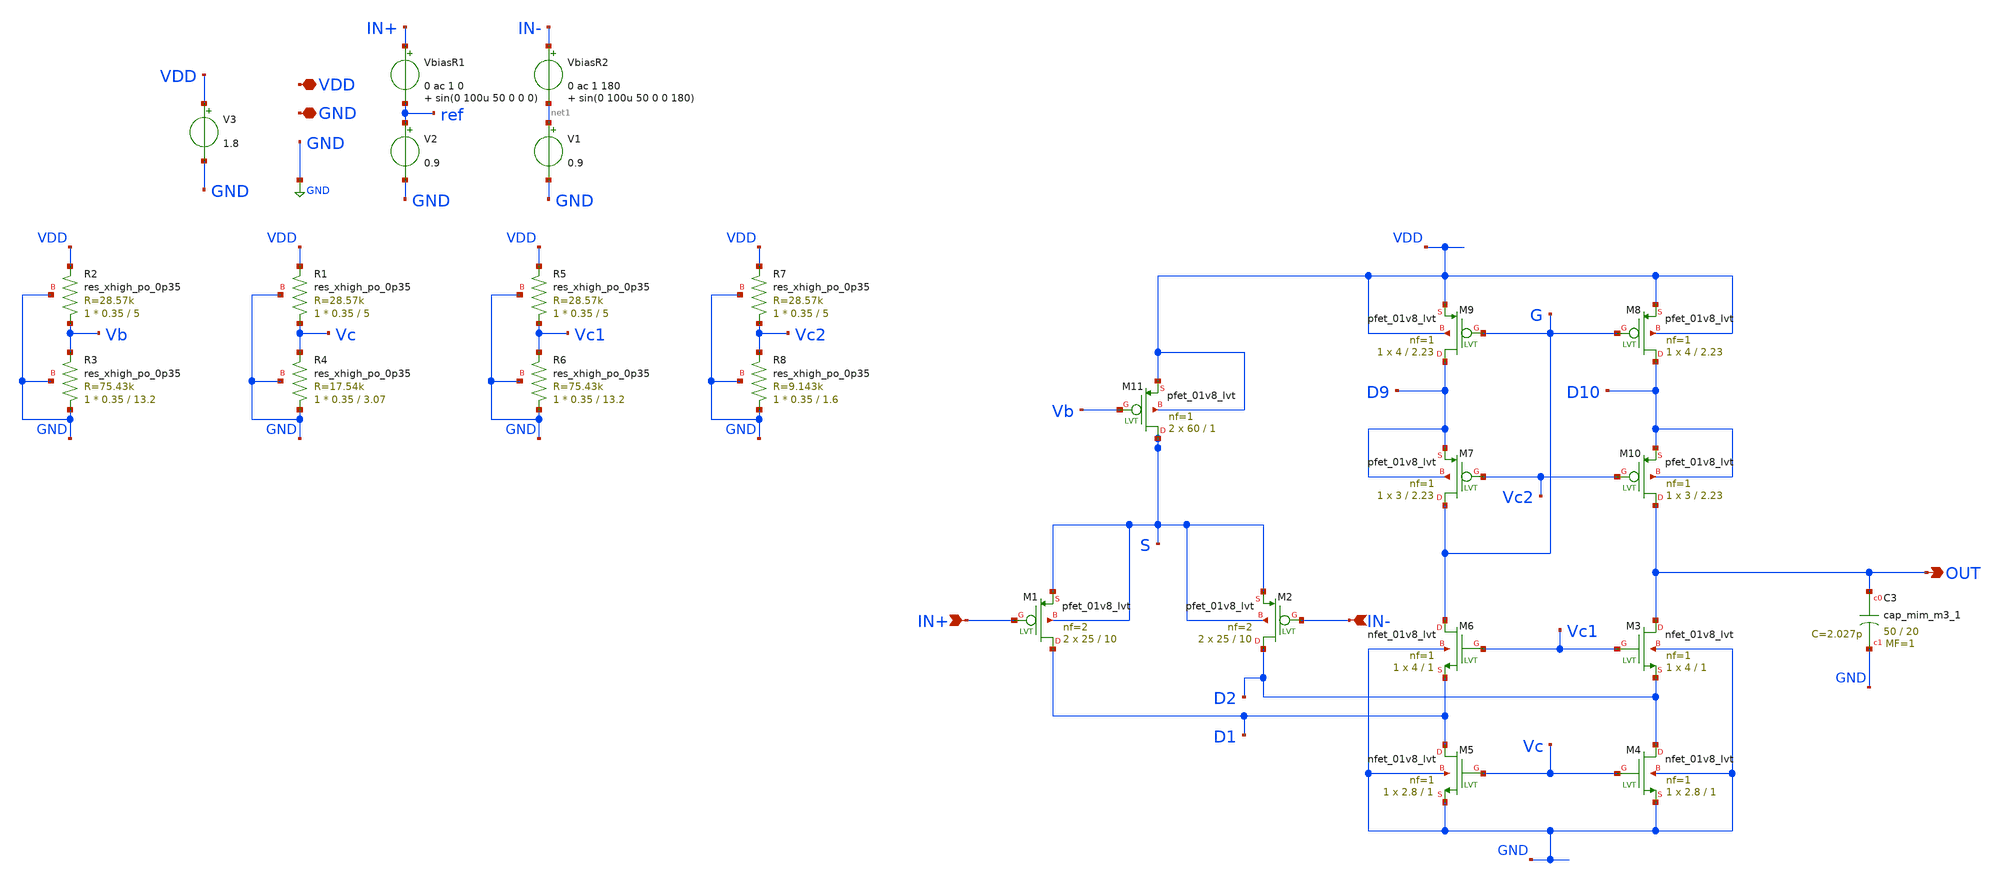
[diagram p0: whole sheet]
** sch_path: xschem/OTA_FoldedCascode_AC1_PVT.sch
**.subckt OTA_FoldedCascode_AC1_PVT VDD GND OUT IN+ IN-
*.iopin VDD
*.iopin GND
*.opin OUT
*.ipin IN+
*.ipin IN-
VbiasR1 IN+ ref 0 ac 1 0 sin(0 100u 50 0 0 0)
V2 ref GND 0.9
V3 VDD GND 1.8
XC3 OUT GND sky130_fd_pr__cap_mim_m3_1 W=50 L=20 MF=1 m=1
XM11 S Vb VDD VDD sky130_fd_pr__pfet_01v8_lvt L=1 W=60 nf=1 ad='int((nf+1)/2) * W/nf * 0.29' as='int((nf+2)/2) * W/nf * 0.29'
+ pd='2*int((nf+1)/2) * (W/nf + 0.29)' ps='2*int((nf+2)/2) * (W/nf + 0.29)' nrd='0.29 / W' nrs='0.29 / W'
+ sa=0 sb=0 sd=0 mult=2 m=2
XM1 D1 IN+ S S sky130_fd_pr__pfet_01v8_lvt L=10 W=25 nf=2 ad='int((nf+1)/2) * W/nf * 0.29' as='int((nf+2)/2) * W/nf * 0.29'
+ pd='2*int((nf+1)/2) * (W/nf + 0.29)' ps='2*int((nf+2)/2) * (W/nf + 0.29)' nrd='0.29 / W' nrs='0.29 / W'
+ sa=0 sb=0 sd=0 mult=2 m=2
XM2 D2 IN- S S sky130_fd_pr__pfet_01v8_lvt L=10 W=25 nf=2 ad='int((nf+1)/2) * W/nf * 0.29' as='int((nf+2)/2) * W/nf * 0.29'
+ pd='2*int((nf+1)/2) * (W/nf + 0.29)' ps='2*int((nf+2)/2) * (W/nf + 0.29)' nrd='0.29 / W' nrs='0.29 / W'
+ sa=0 sb=0 sd=0 mult=2 m=2
XM3 OUT Vc1 D2 GND sky130_fd_pr__nfet_01v8_lvt L=1 W=4 nf=1 ad='int((nf+1)/2) * W/nf * 0.29' as='int((nf+2)/2) * W/nf * 0.29'
+ pd='2*int((nf+1)/2) * (W/nf + 0.29)' ps='2*int((nf+2)/2) * (W/nf + 0.29)' nrd='0.29 / W' nrs='0.29 / W'
+ sa=0 sb=0 sd=0 mult=1 m=1
XM4 D2 Vc GND GND sky130_fd_pr__nfet_01v8_lvt L=1 W=2.8 nf=1 ad='int((nf+1)/2) * W/nf * 0.29' as='int((nf+2)/2) * W/nf * 0.29'
+ pd='2*int((nf+1)/2) * (W/nf + 0.29)' ps='2*int((nf+2)/2) * (W/nf + 0.29)' nrd='0.29 / W' nrs='0.29 / W'
+ sa=0 sb=0 sd=0 mult=1 m=1
XM5 D1 Vc GND GND sky130_fd_pr__nfet_01v8_lvt L=1 W=2.8 nf=1 ad='int((nf+1)/2) * W/nf * 0.29' as='int((nf+2)/2) * W/nf * 0.29'
+ pd='2*int((nf+1)/2) * (W/nf + 0.29)' ps='2*int((nf+2)/2) * (W/nf + 0.29)' nrd='0.29 / W' nrs='0.29 / W'
+ sa=0 sb=0 sd=0 mult=1 m=1
XM6 G Vc1 D1 GND sky130_fd_pr__nfet_01v8_lvt L=1 W=4 nf=1 ad='int((nf+1)/2) * W/nf * 0.29' as='int((nf+2)/2) * W/nf * 0.29'
+ pd='2*int((nf+1)/2) * (W/nf + 0.29)' ps='2*int((nf+2)/2) * (W/nf + 0.29)' nrd='0.29 / W' nrs='0.29 / W'
+ sa=0 sb=0 sd=0 mult=1 m=1
XM7 G Vc2 D9 D9 sky130_fd_pr__pfet_01v8_lvt L=2.23 W=3 nf=1 ad='int((nf+1)/2) * W/nf * 0.29' as='int((nf+2)/2) * W/nf * 0.29'
+ pd='2*int((nf+1)/2) * (W/nf + 0.29)' ps='2*int((nf+2)/2) * (W/nf + 0.29)' nrd='0.29 / W' nrs='0.29 / W'
+ sa=0 sb=0 sd=0 mult=1 m=1
XM9 D9 G VDD VDD sky130_fd_pr__pfet_01v8_lvt L=2.23 W=4 nf=1 ad='int((nf+1)/2) * W/nf * 0.29' as='int((nf+2)/2) * W/nf * 0.29'
+ pd='2*int((nf+1)/2) * (W/nf + 0.29)' ps='2*int((nf+2)/2) * (W/nf + 0.29)' nrd='0.29 / W' nrs='0.29 / W'
+ sa=0 sb=0 sd=0 mult=1 m=1
XM8 D10 G VDD VDD sky130_fd_pr__pfet_01v8_lvt L=2.23 W=4 nf=1 ad='int((nf+1)/2) * W/nf * 0.29' as='int((nf+2)/2) * W/nf * 0.29'
+ pd='2*int((nf+1)/2) * (W/nf + 0.29)' ps='2*int((nf+2)/2) * (W/nf + 0.29)' nrd='0.29 / W' nrs='0.29 / W'
+ sa=0 sb=0 sd=0 mult=1 m=1
XM10 OUT Vc2 D10 D10 sky130_fd_pr__pfet_01v8_lvt L=2.23 W=3 nf=1 ad='int((nf+1)/2) * W/nf * 0.29' as='int((nf+2)/2) * W/nf * 0.29'
+ pd='2*int((nf+1)/2) * (W/nf + 0.29)' ps='2*int((nf+2)/2) * (W/nf + 0.29)' nrd='0.29 / W' nrs='0.29 / W'
+ sa=0 sb=0 sd=0 mult=1 m=1
VbiasR2 IN- net1 0 ac 1 180 sin(0 100u 50 0 0 180)
V1 net1 GND 0.9
XR2 Vb VDD GND sky130_fd_pr__res_xhigh_po_0p35 L=5 mult=1 m=1
XR3 GND Vb GND sky130_fd_pr__res_xhigh_po_0p35 L=13.2 mult=1 m=1
XR1 Vc VDD GND sky130_fd_pr__res_xhigh_po_0p35 L=5 mult=1 m=1
XR4 GND Vc GND sky130_fd_pr__res_xhigh_po_0p35 L=3.07 mult=1 m=1
XR5 Vc1 VDD GND sky130_fd_pr__res_xhigh_po_0p35 L=5 mult=1 m=1
XR6 GND Vc1 GND sky130_fd_pr__res_xhigh_po_0p35 L=13.2 mult=1 m=1
XR7 Vc2 VDD GND sky130_fd_pr__res_xhigh_po_0p35 L=5 mult=1 m=1
XR8 GND Vc2 GND sky130_fd_pr__res_xhigh_po_0p35 L=1.6 mult=1 m=1
**** begin user architecture code



.control
    set wr_vecnames
    set wr_singlescale

    let pvt_runs = 3
    let run = 1

    dowhile run <= pvt_runs
        if (run = 1)
            echo >>> SCENARIO 1: TYPICAL (27C, V3 1.8V)
            set temp = 27
            alter V3 1.8
        end

        if (run = 2)
            echo >>> SCENARIO 2: HOT & LOW (125C, V3 1.62V)
            set temp = 125
            alter V3 1.62
        end

        if (run = 3)
            echo >>> SCENARIO 3: COLD & HIGH (-40C, V3 1.98V)
            set temp = -40
            alter V3 1.98
        end

        * Simulazione AC: decade, 10 punti, da 1Hz a 100MHz
        ac dec 10 1 100meg

        let run = run + 1
    end

    * Impostiamo il plot AC per vedere la scala in frequenza correttamente
    setplot ac1

    * Plot del guadagno in dB
    plot db(ac1.v(OUT)) db(ac2.v(OUT)) db(ac3.v(OUT)) title 'AC Gain PVT Corners'

    * Plot della fase
    plot ph(ac1.v(OUT)) ph(ac2.v(OUT)) ph(ac3.v(OUT)) title 'AC Phase PVT Corners'
.endc



.lib $::SKYWATER_MODELS/sky130.lib.spice tt
**** end user architecture code
**.ends
.GLOBAL GND
.end
